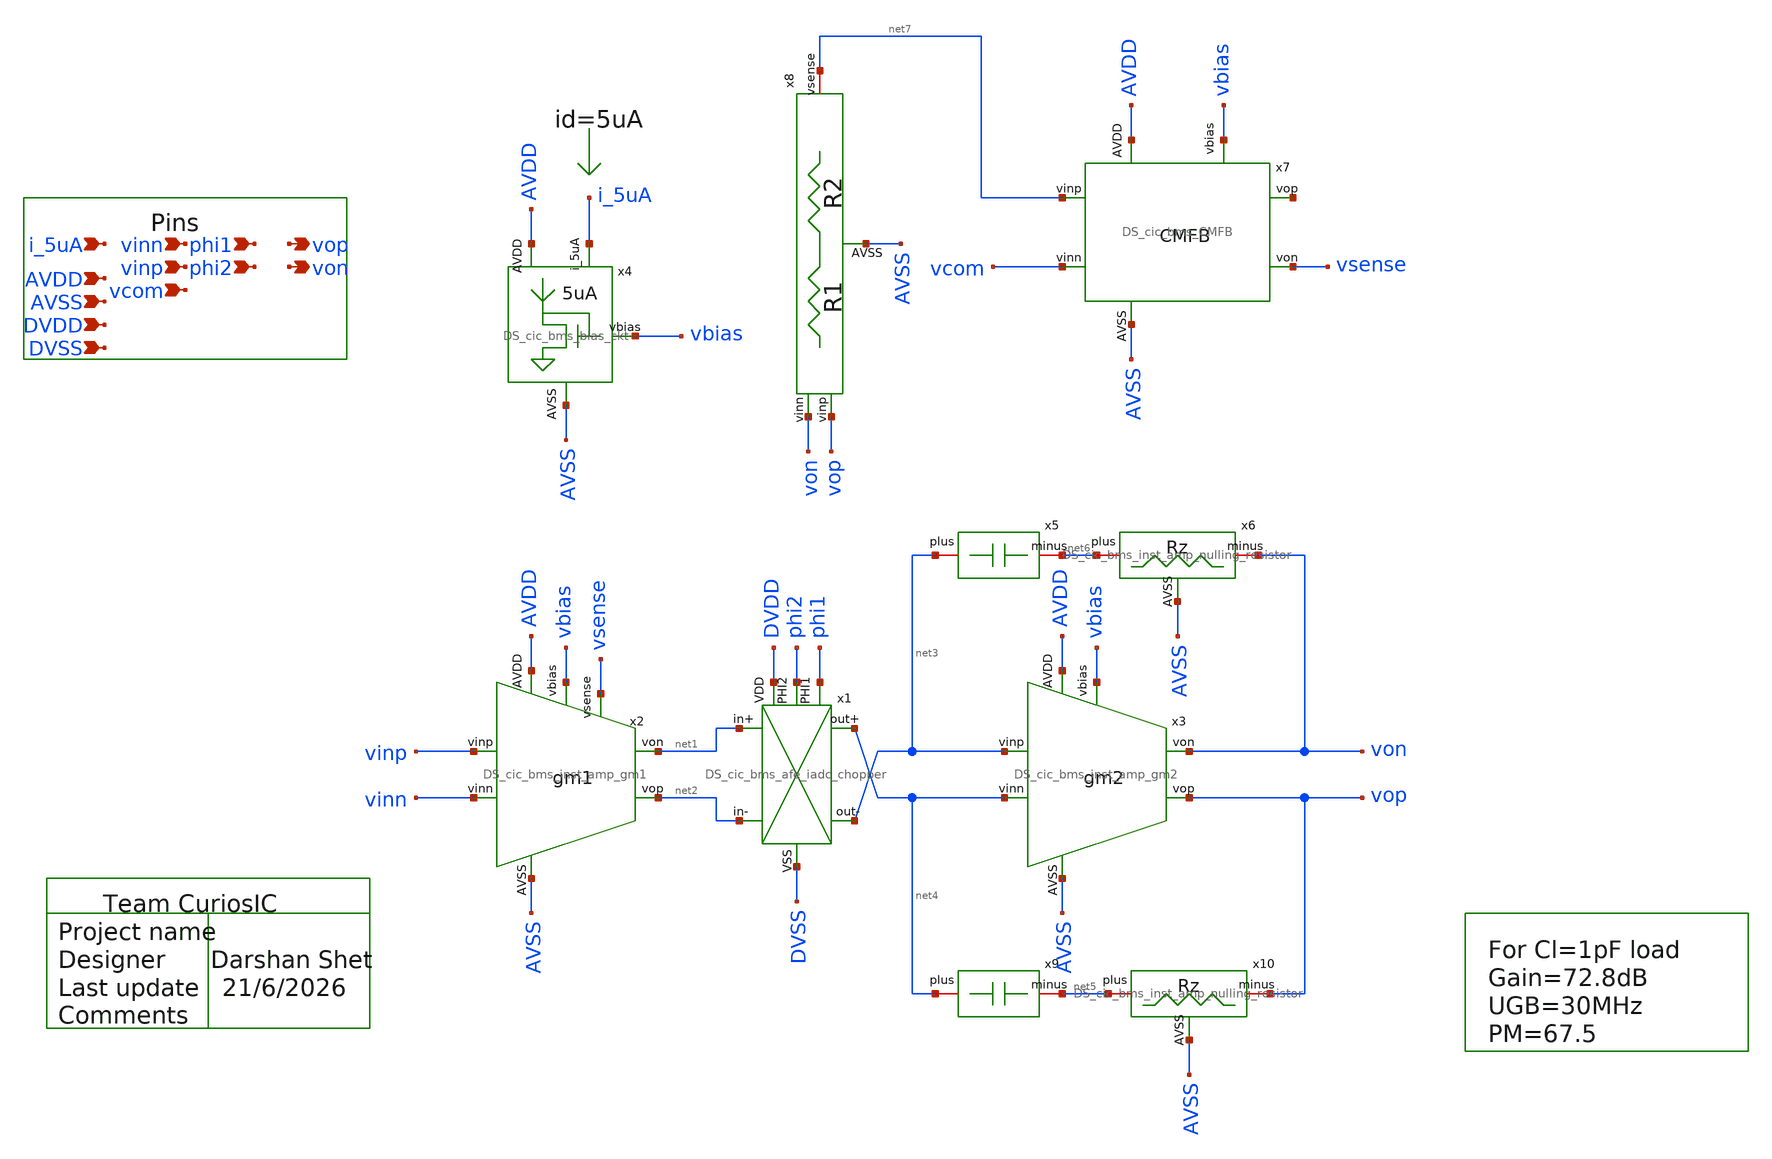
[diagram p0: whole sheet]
** sch_path: design/schematics/CCIA/Instrumentation Amplifier/top/DS_cic_bms_inst_amp_IA.sch
**.subckt DS_cic_bms_inst_amp_IA i_5uA AVDD AVSS vinn vinp vcom phi1 phi2 vop von DVDD DVSS
*.ipin i_5uA
*.ipin AVDD
*.ipin AVSS
*.ipin vinn
*.ipin vinp
*.ipin vcom
*.ipin phi1
*.ipin phi2
*.opin vop
*.opin von
*.ipin DVDD
*.ipin DVSS
x1 DVDD DVSS net1 net2 phi1 phi2 net4 net3 DS_cic_bms_afe_iadc_chopper
x4 i_5uA AVSS AVDD vbias DS_cic_bms_bias_ckt
x7 AVDD AVSS vcom net7 vbias net8 vsense DS_cic_bms_CMFB
x8 von net7 vop AVSS DS_cic_bms_CMFB_res_div
x9 net4 net5 DS_cic_bms_inst_amp_miller_cap
x10 net5 vop AVSS DS_cic_bms_inst_amp_nulling_resistor
x5 net3 net6 DS_cic_bms_inst_amp_miller_cap
x6 net6 von AVSS DS_cic_bms_inst_amp_nulling_resistor
x2 net2 AVDD vinp vinn AVSS net1 vsense vbias DS_cic_bms_inst_amp_gm1
x3 net3 AVDD vop net4 AVSS von vbias DS_cic_bms_inst_amp_gm2
**.ends
.end
